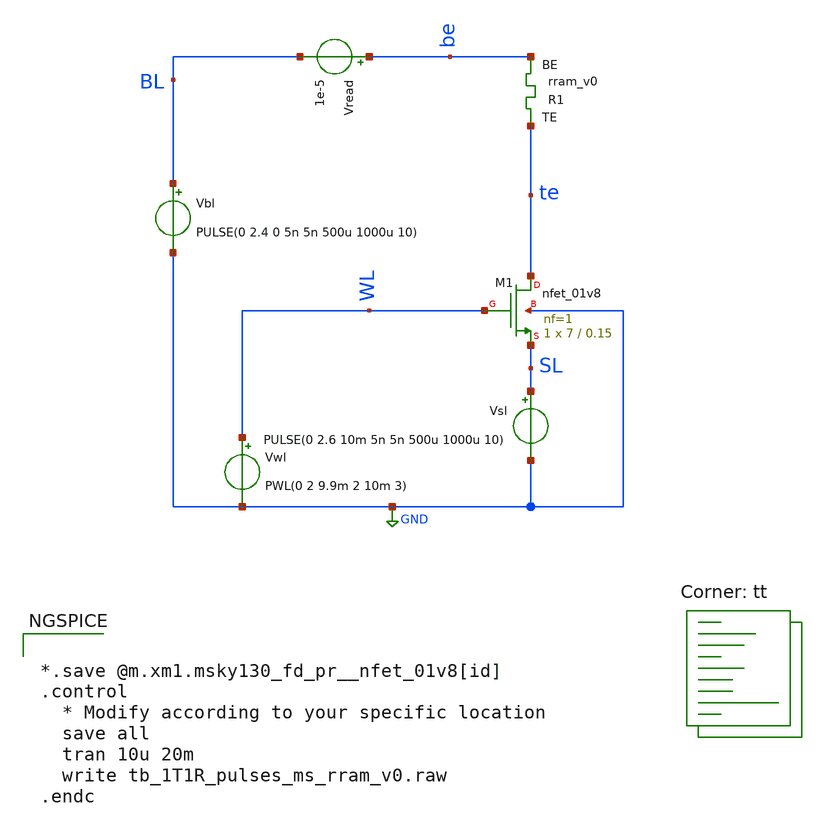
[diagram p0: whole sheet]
** sch_path: memristor_models/wellposed/tb_1T1R_pulses_ms_rram_v0.sch
**.subckt tb_1T1R_pulses_ms_rram_v0
XM1 te WL SL GND sky130_fd_pr__nfet_01v8 L=0.15 W=7 nf=1 ad='int((nf+1)/2) * W/nf * 0.29' as='int((nf+2)/2) * W/nf * 0.29'
+ pd='2*int((nf+1)/2) * (W/nf + 0.29)' ps='2*int((nf+2)/2) * (W/nf + 0.29)' nrd='0.29 / W' nrs='0.29 / W'
+ sa=0 sb=0 sd=0 mult=1 m=1
Vwl WL GND PWL(0 2 9.9m 2 10m 3)
Vbl BL GND PULSE(0 2.4 0 5n 5n 500u 1000u 10)
Vread be BL 1e-5
XR1 te be rram_v0
Vsl SL GND PULSE(0 2.6 10m 5n 5n 500u 1000u 10)
**** begin user architecture code


*.save @m.xm1.msky130_fd_pr__nfet_01v8[id]
.control
  * Modify according to your specific location
  save all
  tran 10u 20m
  write tb_1T1R_pulses_ms_rram_v0.raw
.endc



.lib $::SKYWATER_MODELS/sky130.lib.spice tt

** opencircuitdesign pdks install
.inc $::SKYWATER_MODELS/rram_v0.spice

**** end user architecture code
**.ends
.GLOBAL GND
.end
